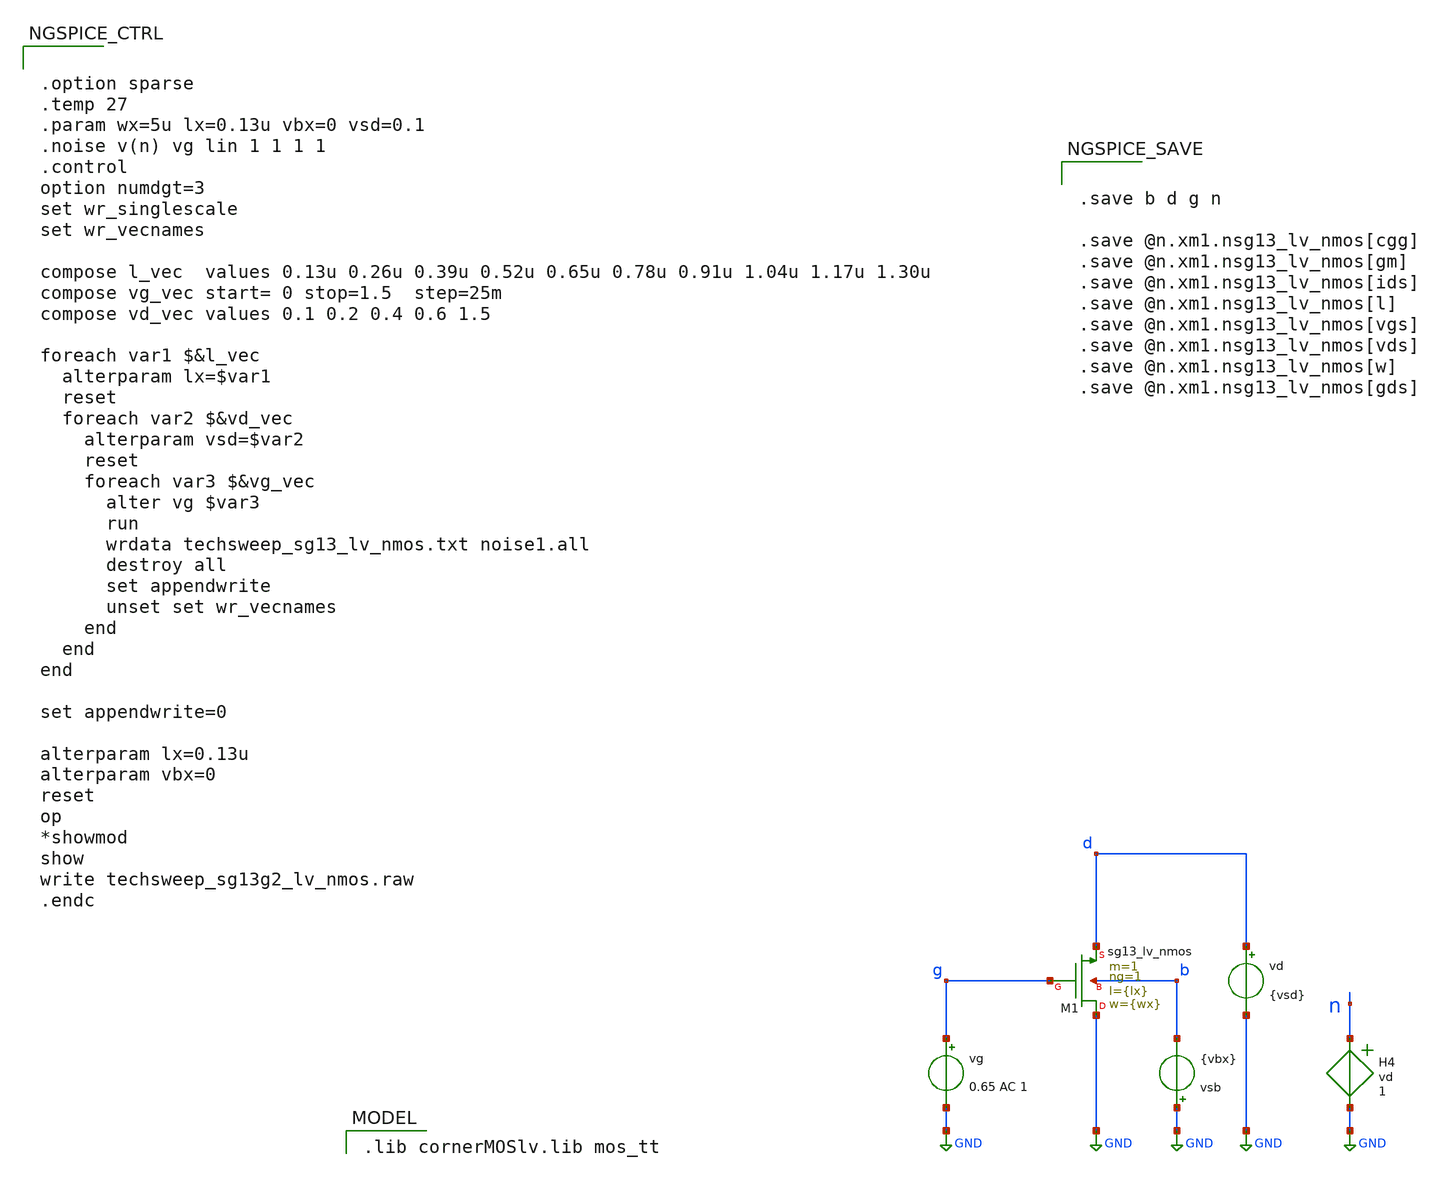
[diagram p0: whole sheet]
** sch_path: nmos.sch
* (c) 2024 Harald Pretl (adapted from Boris Murmann)
**.subckt nmos
vg g GND 0.65 AC 1
vd d GND {vsd}
XM1 GND g d b sg13_lv_nmos w={wx} l={lx} ng=1 m=1 mm_ok=1
vsb GND b {vbx}
H4 n GND vd 1
**** begin user architecture code
 .lib cornerMOSlv.lib mos_tt



.option sparse
.temp 27
.param wx=5u lx=0.13u vbx=0 vsd=0.1
.noise v(n) vg lin 1 1 1 1
.control
option numdgt=3
set wr_singlescale
set wr_vecnames

compose l_vec  values 0.13u 0.26u 0.39u 0.52u 0.65u 0.78u 0.91u 1.04u 1.17u 1.30u
compose vg_vec start= 0 stop=1.5  step=25m
compose vd_vec values 0.1 0.2 0.4 0.6 1.5

foreach var1 $&l_vec
  alterparam lx=$var1
  reset
  foreach var2 $&vd_vec
    alterparam vsd=$var2
    reset
    foreach var3 $&vg_vec
      alter vg $var3
      run
      wrdata techsweep_sg13_lv_nmos.txt noise1.all
      destroy all
      set appendwrite
      unset set wr_vecnames
    end
  end
end

set appendwrite=0

alterparam lx=0.13u
alterparam vbx=0
reset
op
*showmod
show
write techsweep_sg13g2_lv_nmos.raw
.endc




.save b d g n

.save @n.xm1.nsg13_lv_nmos[cgg]
.save @n.xm1.nsg13_lv_nmos[gm]
.save @n.xm1.nsg13_lv_nmos[ids]
.save @n.xm1.nsg13_lv_nmos[l]
.save @n.xm1.nsg13_lv_nmos[vgs]
.save @n.xm1.nsg13_lv_nmos[vds]
.save @n.xm1.nsg13_lv_nmos[w]
.save @n.xm1.nsg13_lv_nmos[gds]




**** end user architecture code
**.ends
.GLOBAL GND
.end
